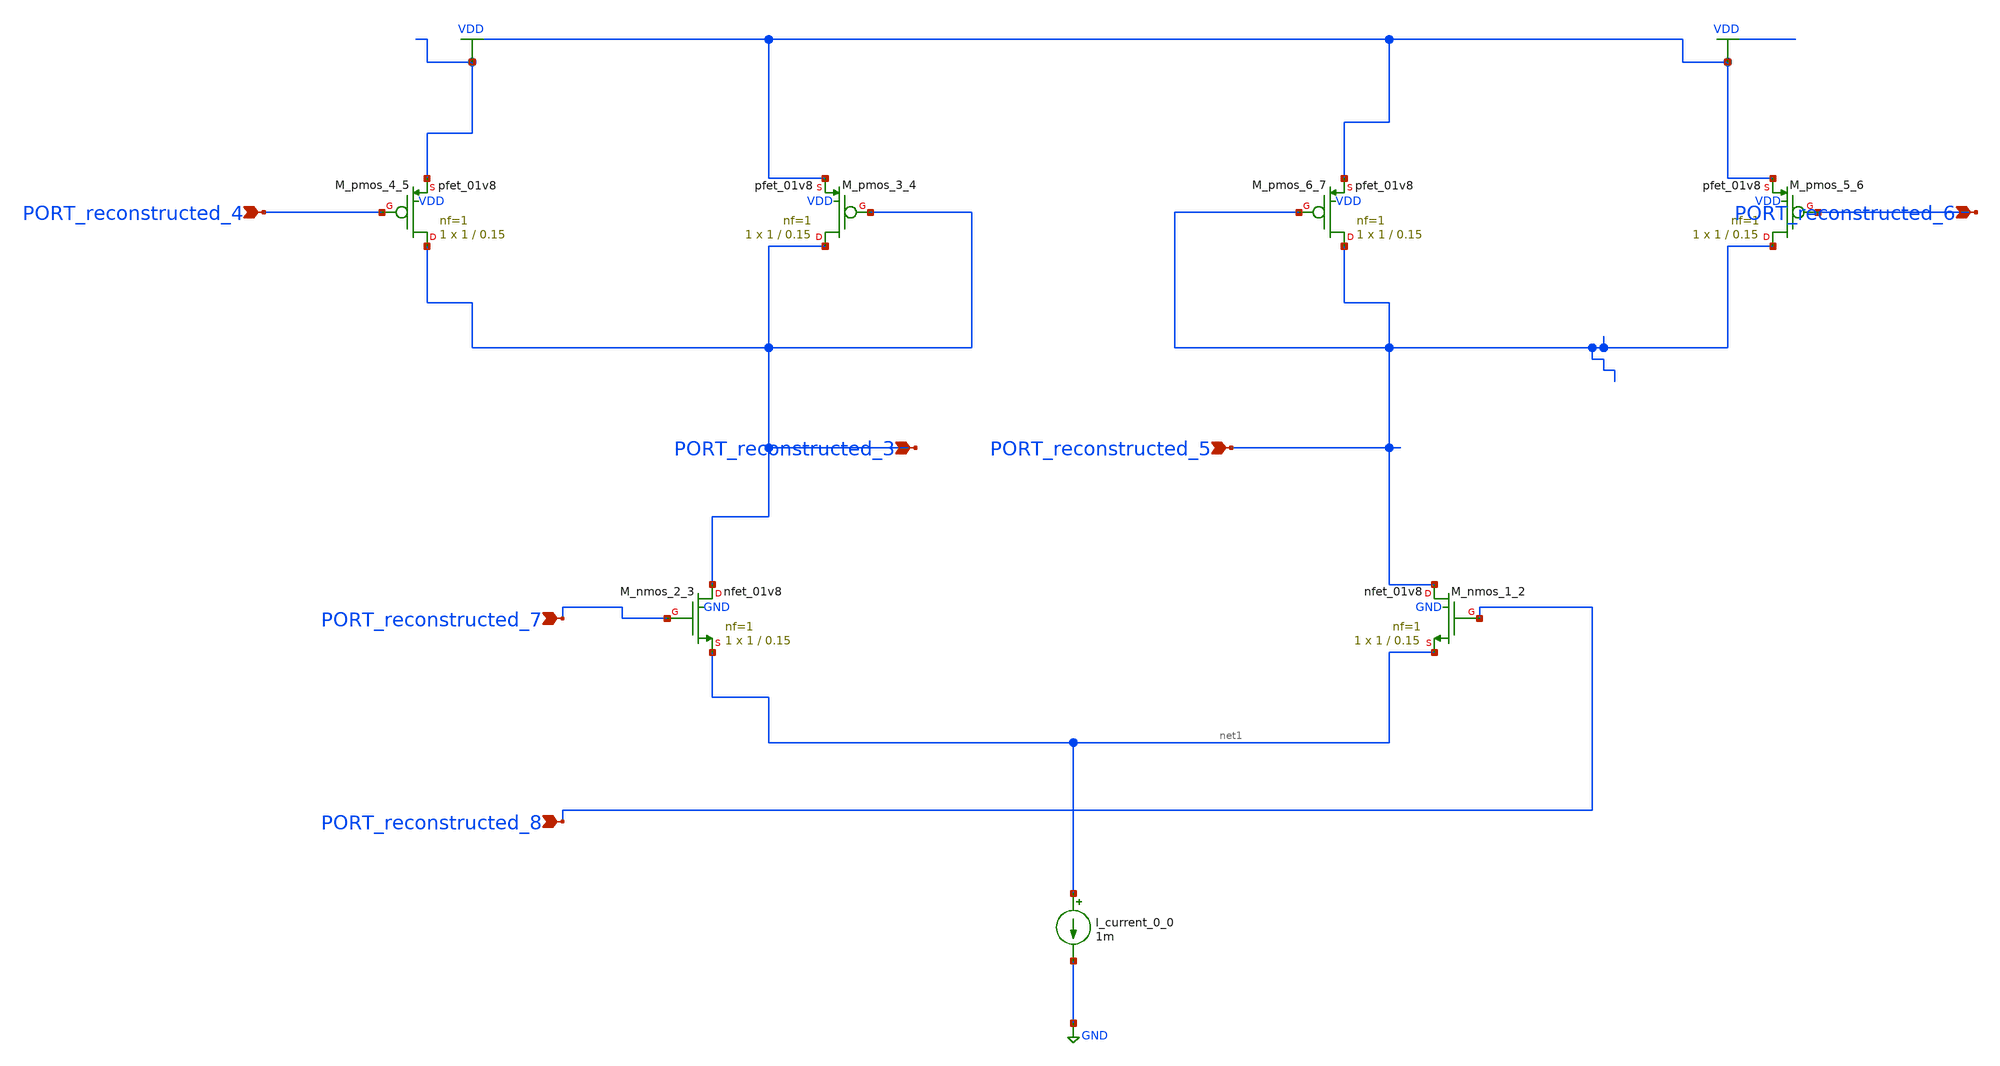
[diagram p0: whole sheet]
** sch_path: schematics/AMSNet/224.sch
**.subckt 224 PORT_reconstructed_7 PORT_reconstructed_6 PORT_reconstructed_4 PORT_reconstructed_8
*+ PORT_reconstructed_3 PORT_reconstructed_5
*.ipin PORT_reconstructed_7
*.ipin PORT_reconstructed_6
*.ipin PORT_reconstructed_4
*.ipin PORT_reconstructed_8
*.ipin PORT_reconstructed_3
*.ipin PORT_reconstructed_5
I_current_0_0 net1 GND 1m
XM_nmos_1_2 PORT_reconstructed_5 PORT_reconstructed_8 net1 GND sky130_fd_pr__nfet_01v8 L=0.15 W=1 nf=1
+ ad='int((1 + 1)/2) * 1 / 1 * 0.29' as='int((1 + 2)/2) * 1 / 1 * 0.29' pd='2*int((1 + 1)/2) * (1 / 1 + 0.29)'
+ ps='2*int((1 + 2)/2) * (1 / 1 + 0.29)' nrd='0.29 / 1 ' nrs='0.29 / 1 ' sa=0 sb=0 sd=0 mult=1 m=1
XM_nmos_2_3 PORT_reconstructed_3 PORT_reconstructed_7 net1 GND sky130_fd_pr__nfet_01v8 L=0.15 W=1 nf=1
+ ad='int((1 + 1)/2) * 1 / 1 * 0.29' as='int((1 + 2)/2) * 1 / 1 * 0.29' pd='2*int((1 + 1)/2) * (1 / 1 + 0.29)'
+ ps='2*int((1 + 2)/2) * (1 / 1 + 0.29)' nrd='0.29 / 1 ' nrs='0.29 / 1 ' sa=0 sb=0 sd=0 mult=1 m=1
XM_pmos_3_4 PORT_reconstructed_3 PORT_reconstructed_3 VDD VDD sky130_fd_pr__pfet_01v8 L=0.15 W=1 nf=1
+ ad='int((1 + 1)/2) * 1 / 1 * 0.29' as='int((1 + 2)/2) * 1 / 1 * 0.29' pd='2*int((1 + 1)/2) * (1 / 1 + 0.29)'
+ ps='2*int((1 + 2)/2) * (1 / 1 + 0.29)' nrd='0.29 / 1 ' nrs='0.29 / 1 ' sa=0 sb=0 sd=0 mult=1 m=1
XM_pmos_4_5 PORT_reconstructed_3 PORT_reconstructed_4 VDD VDD sky130_fd_pr__pfet_01v8 L=0.15 W=1 nf=1
+ ad='int((1 + 1)/2) * 1 / 1 * 0.29' as='int((1 + 2)/2) * 1 / 1 * 0.29' pd='2*int((1 + 1)/2) * (1 / 1 + 0.29)'
+ ps='2*int((1 + 2)/2) * (1 / 1 + 0.29)' nrd='0.29 / 1 ' nrs='0.29 / 1 ' sa=0 sb=0 sd=0 mult=1 m=1
XM_pmos_5_6 PORT_reconstructed_5 PORT_reconstructed_6 VDD VDD sky130_fd_pr__pfet_01v8 L=0.15 W=1 nf=1
+ ad='int((1 + 1)/2) * 1 / 1 * 0.29' as='int((1 + 2)/2) * 1 / 1 * 0.29' pd='2*int((1 + 1)/2) * (1 / 1 + 0.29)'
+ ps='2*int((1 + 2)/2) * (1 / 1 + 0.29)' nrd='0.29 / 1 ' nrs='0.29 / 1 ' sa=0 sb=0 sd=0 mult=1 m=1
XM_pmos_6_7 PORT_reconstructed_5 PORT_reconstructed_5 VDD VDD sky130_fd_pr__pfet_01v8 L=0.15 W=1 nf=1
+ ad='int((1 + 1)/2) * 1 / 1 * 0.29' as='int((1 + 2)/2) * 1 / 1 * 0.29' pd='2*int((1 + 1)/2) * (1 / 1 + 0.29)'
+ ps='2*int((1 + 2)/2) * (1 / 1 + 0.29)' nrd='0.29 / 1 ' nrs='0.29 / 1 ' sa=0 sb=0 sd=0 mult=1 m=1
**.ends
.GLOBAL GND
.GLOBAL VDD
.end
